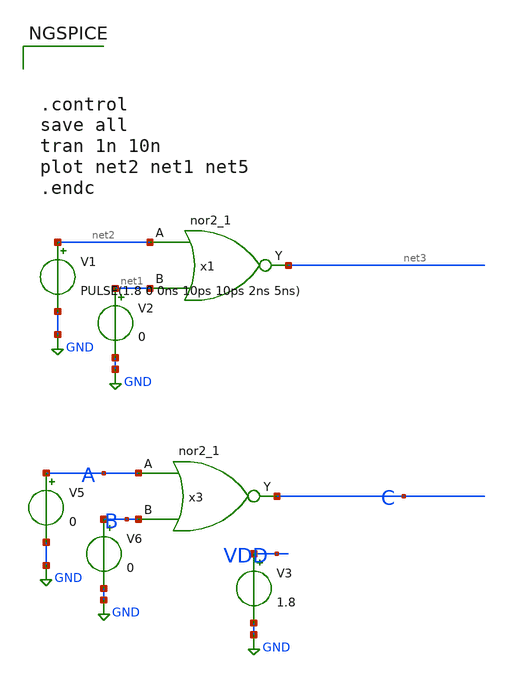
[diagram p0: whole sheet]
** sch_path: xiaolin/norsingle_tb.sch
**.subckt norsingle_tb
x1 net2 net1 GND GND VDD VDD net3 sky130_fd_sc_hd__nor2_1
V1 net2 GND PULSE(1.8 0 0ns 10ps 10ps 2ns 5ns)
V2 net1 GND 0
x3 A B GND GND VDD VDD C sky130_fd_sc_hd__nor2_1
V5 A GND 0
V6 B GND 0
V3 VDD GND 1.8
**** begin user architecture code


.lib /farmshare/home/classes/ee/372/PDKs/open_pdks/sky130/sky130A/libs.tech/ngspice/sky130.lib.spice tt
.include /farmshare/home/classes/ee/372/PDKs/open_pdks/sky130/sky130A/libs.ref/sky130_fd_sc_hd/spice/sky130_fd_sc_hd.spice






.control
save all
tran 1n 10n
plot net2 net1 net5
.endc


**** end user architecture code
**.ends
.GLOBAL GND
.end
